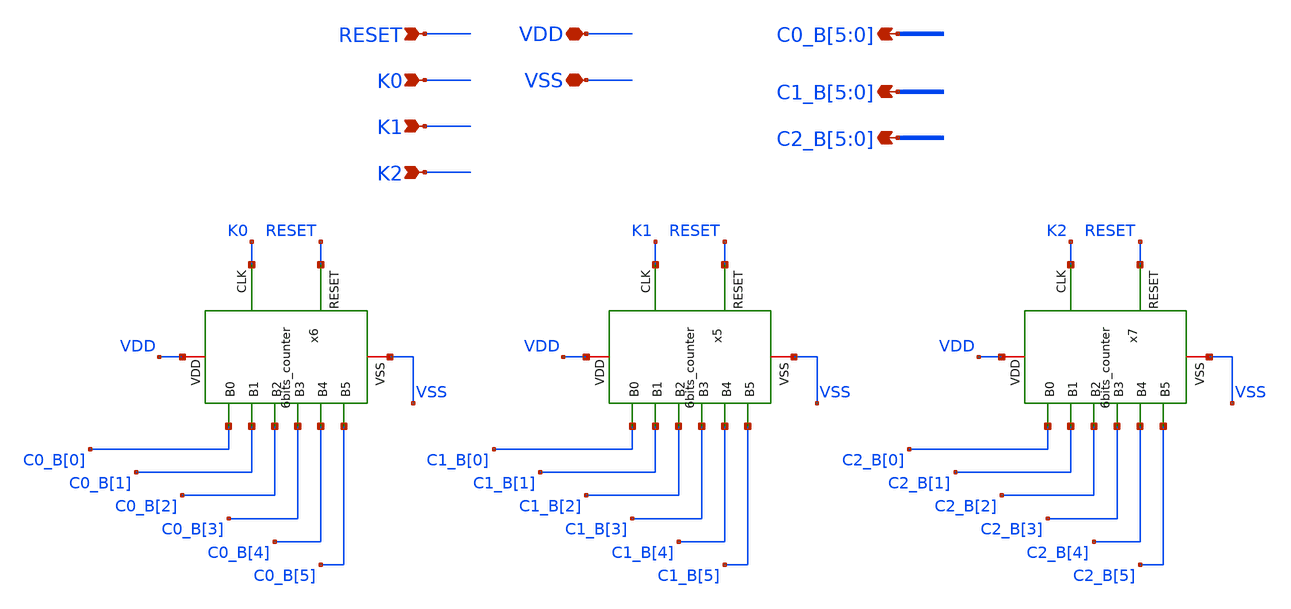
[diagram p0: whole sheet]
** sch_path: 27_03_26/TOP_MAXI/Esquematicos/Counters_6bits.sch
**.subckt Counters_6bits VDD VSS K0 K1 K2 RESET C0_B[5],C0_B[4],C0_B[3],C0_B[2],C0_B[1],C0_B[0]
*+ C1_B[5],C1_B[4],C1_B[3],C1_B[2],C1_B[1],C1_B[0] C2_B[5],C2_B[4],C2_B[3],C2_B[2],C2_B[1],C2_B[0]
*.iopin VDD
*.iopin VSS
*.ipin K0
*.ipin K1
*.ipin K2
*.ipin RESET
*.opin C0_B[5],C0_B[4],C0_B[3],C0_B[2],C0_B[1],C0_B[0]
*.opin C1_B[5],C1_B[4],C1_B[3],C1_B[2],C1_B[1],C1_B[0]
*.opin C2_B[5],C2_B[4],C2_B[3],C2_B[2],C2_B[1],C2_B[0]
x5 C1_B[0] K1 VDD C1_B[1] C1_B[2] VSS RESET C1_B[3] C1_B[4] C1_B[5] 6bits_counter
x6 C0_B[0] K0 VDD C0_B[1] C0_B[2] VSS RESET C0_B[3] C0_B[4] C0_B[5] 6bits_counter
x7 C2_B[0] K2 VDD C2_B[1] C2_B[2] VSS RESET C2_B[3] C2_B[4] C2_B[5] 6bits_counter
**.ends
.end
